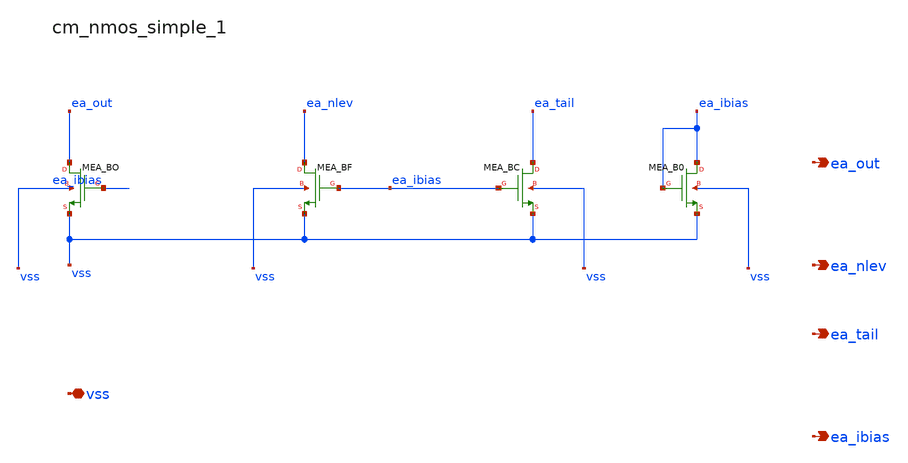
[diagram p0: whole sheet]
** sch_path: analog-db/raw/ldo_005_buffered_ref/hier/blocks/cm_nmos_simple_1.sch
**.subckt cm_nmos_simple_1 vss ea_out ea_nlev ea_tail ea_ibias
*.iopin vss
*.opin ea_out
*.opin ea_nlev
*.opin ea_tail
*.opin ea_ibias
XMEA_B0 ea_ibias ea_ibias vss vss sg13_hv_nmos w=x_dut_xmea_b0_w l=x_dut_xmea_b0_l ng=1 m=1
XMEA_BC ea_tail ea_ibias vss vss sg13_hv_nmos w=x_dut_xmea_bc_w l=x_dut_xmea_bc_l ng=1 m=1
XMEA_BF ea_nlev ea_ibias vss vss sg13_hv_nmos w=x_dut_xmea_bf_w l=x_dut_xmea_bf_l ng=1 m=1
XMEA_BO ea_out ea_ibias vss vss sg13_hv_nmos w=x_dut_xmea_bo_w l=x_dut_xmea_bo_l ng=1 m=1
**.ends
.end
